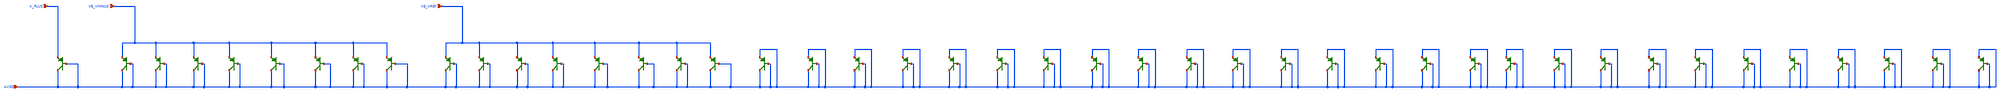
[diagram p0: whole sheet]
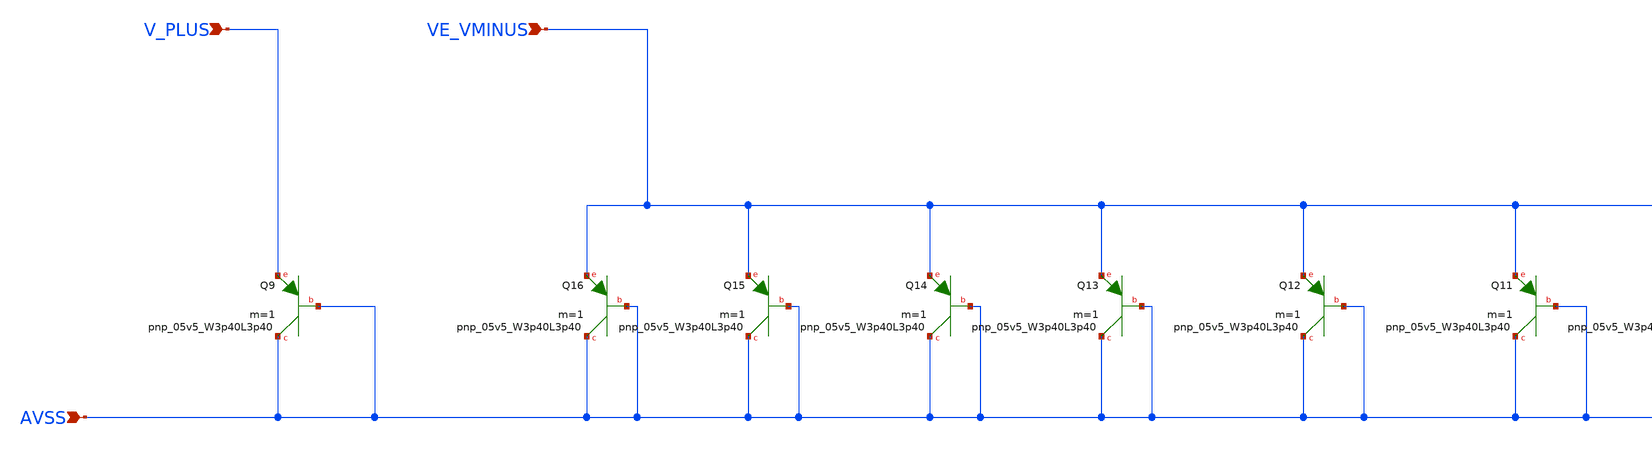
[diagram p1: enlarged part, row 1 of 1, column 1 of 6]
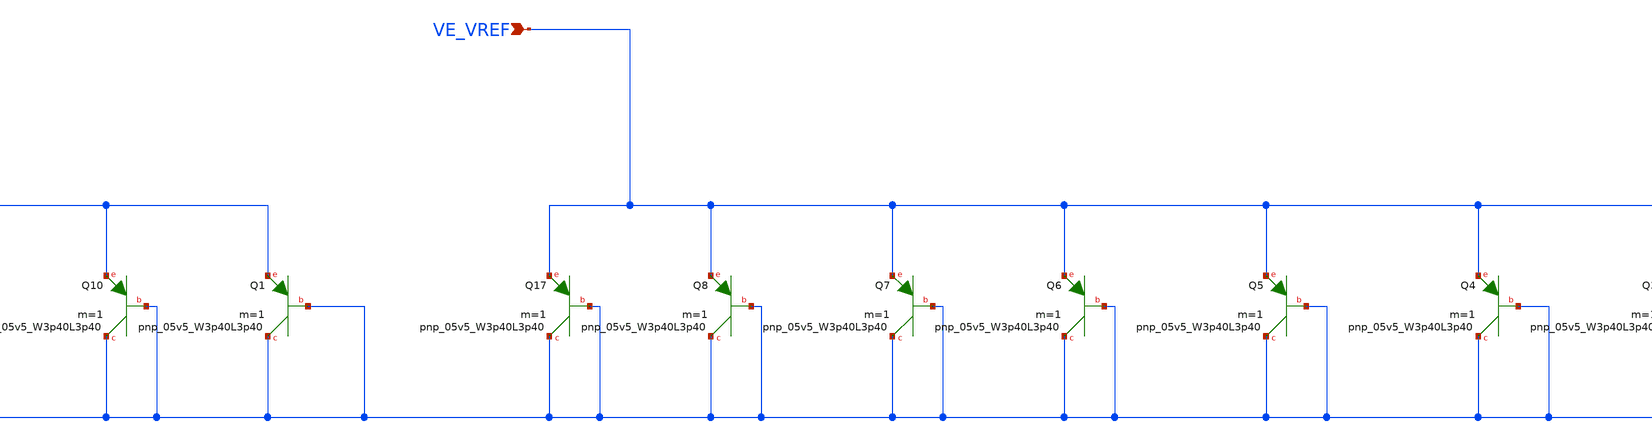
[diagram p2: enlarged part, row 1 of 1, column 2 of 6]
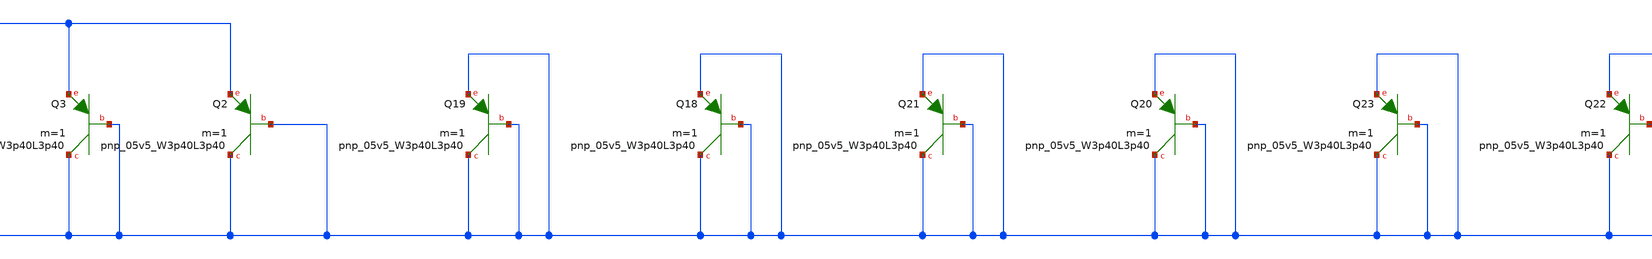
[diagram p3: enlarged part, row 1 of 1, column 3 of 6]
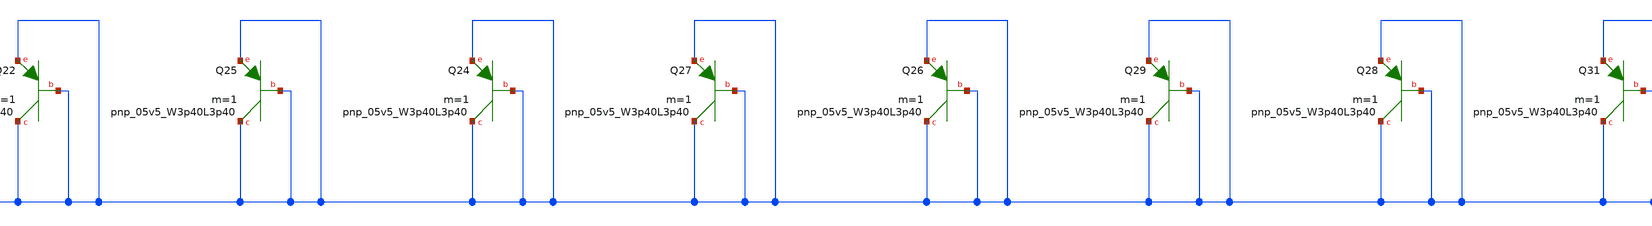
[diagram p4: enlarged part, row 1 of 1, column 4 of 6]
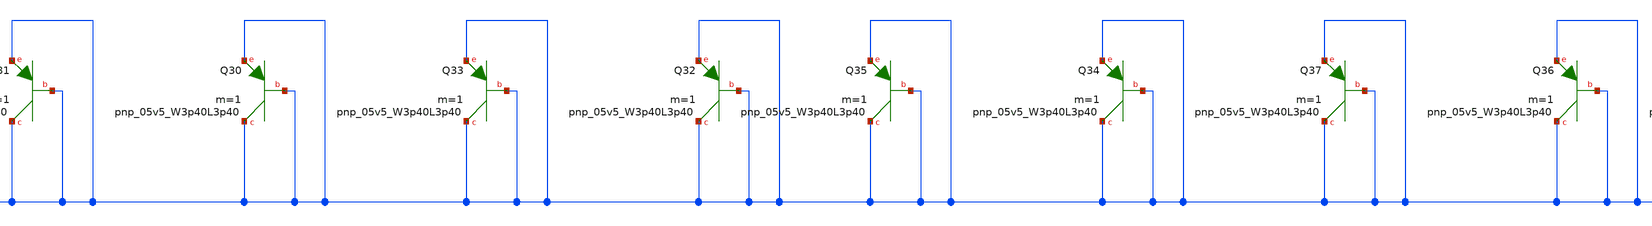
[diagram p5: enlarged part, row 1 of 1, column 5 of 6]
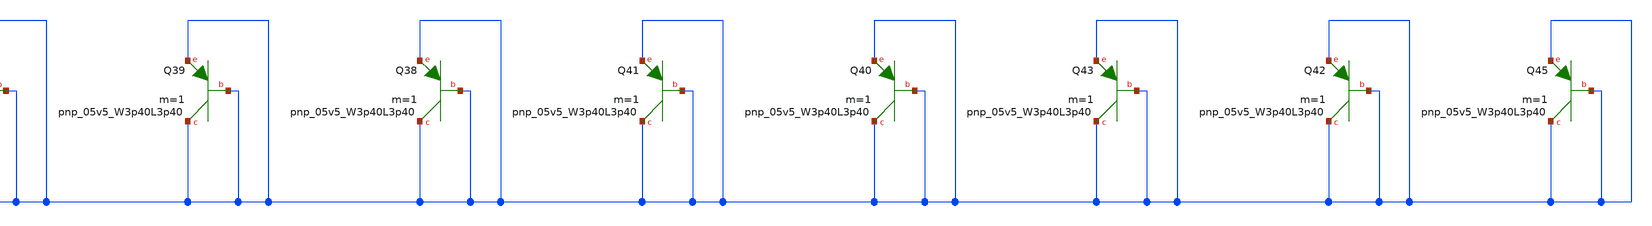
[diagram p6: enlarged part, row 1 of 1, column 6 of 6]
** sch_path: lef/lef/gds/bg2_bjt_array.sch
**.subckt bg2_bjt_array AVSS V_PLUS VE_VMINUS VE_VREF
*.ipin AVSS
*.ipin V_PLUS
*.ipin VE_VMINUS
*.ipin VE_VREF
XQ9 AVSS AVSS V_PLUS sky130_fd_pr__pnp_05v5_W3p40L3p40 m=1
XQ1 AVSS AVSS VE_VMINUS sky130_fd_pr__pnp_05v5_W3p40L3p40 m=1
XQ10 AVSS AVSS VE_VMINUS sky130_fd_pr__pnp_05v5_W3p40L3p40 m=1
XQ11 AVSS AVSS VE_VMINUS sky130_fd_pr__pnp_05v5_W3p40L3p40 m=1
XQ12 AVSS AVSS VE_VMINUS sky130_fd_pr__pnp_05v5_W3p40L3p40 m=1
XQ13 AVSS AVSS VE_VMINUS sky130_fd_pr__pnp_05v5_W3p40L3p40 m=1
XQ14 AVSS AVSS VE_VMINUS sky130_fd_pr__pnp_05v5_W3p40L3p40 m=1
XQ15 AVSS AVSS VE_VMINUS sky130_fd_pr__pnp_05v5_W3p40L3p40 m=1
XQ16 AVSS AVSS VE_VMINUS sky130_fd_pr__pnp_05v5_W3p40L3p40 m=1
XQ2 AVSS AVSS VE_VREF sky130_fd_pr__pnp_05v5_W3p40L3p40 m=1
XQ3 AVSS AVSS VE_VREF sky130_fd_pr__pnp_05v5_W3p40L3p40 m=1
XQ4 AVSS AVSS VE_VREF sky130_fd_pr__pnp_05v5_W3p40L3p40 m=1
XQ5 AVSS AVSS VE_VREF sky130_fd_pr__pnp_05v5_W3p40L3p40 m=1
XQ6 AVSS AVSS VE_VREF sky130_fd_pr__pnp_05v5_W3p40L3p40 m=1
XQ7 AVSS AVSS VE_VREF sky130_fd_pr__pnp_05v5_W3p40L3p40 m=1
XQ8 AVSS AVSS VE_VREF sky130_fd_pr__pnp_05v5_W3p40L3p40 m=1
XQ17 AVSS AVSS VE_VREF sky130_fd_pr__pnp_05v5_W3p40L3p40 m=1
XQ18 AVSS AVSS AVSS sky130_fd_pr__pnp_05v5_W3p40L3p40 m=1
XQ19 AVSS AVSS AVSS sky130_fd_pr__pnp_05v5_W3p40L3p40 m=1
XQ20 AVSS AVSS AVSS sky130_fd_pr__pnp_05v5_W3p40L3p40 m=1
XQ21 AVSS AVSS AVSS sky130_fd_pr__pnp_05v5_W3p40L3p40 m=1
XQ22 AVSS AVSS AVSS sky130_fd_pr__pnp_05v5_W3p40L3p40 m=1
XQ23 AVSS AVSS AVSS sky130_fd_pr__pnp_05v5_W3p40L3p40 m=1
XQ24 AVSS AVSS AVSS sky130_fd_pr__pnp_05v5_W3p40L3p40 m=1
XQ25 AVSS AVSS AVSS sky130_fd_pr__pnp_05v5_W3p40L3p40 m=1
XQ26 AVSS AVSS AVSS sky130_fd_pr__pnp_05v5_W3p40L3p40 m=1
XQ27 AVSS AVSS AVSS sky130_fd_pr__pnp_05v5_W3p40L3p40 m=1
XQ28 AVSS AVSS AVSS sky130_fd_pr__pnp_05v5_W3p40L3p40 m=1
XQ29 AVSS AVSS AVSS sky130_fd_pr__pnp_05v5_W3p40L3p40 m=1
XQ30 AVSS AVSS AVSS sky130_fd_pr__pnp_05v5_W3p40L3p40 m=1
XQ31 AVSS AVSS AVSS sky130_fd_pr__pnp_05v5_W3p40L3p40 m=1
XQ32 AVSS AVSS AVSS sky130_fd_pr__pnp_05v5_W3p40L3p40 m=1
XQ33 AVSS AVSS AVSS sky130_fd_pr__pnp_05v5_W3p40L3p40 m=1
XQ34 AVSS AVSS AVSS sky130_fd_pr__pnp_05v5_W3p40L3p40 m=1
XQ35 AVSS AVSS AVSS sky130_fd_pr__pnp_05v5_W3p40L3p40 m=1
XQ36 AVSS AVSS AVSS sky130_fd_pr__pnp_05v5_W3p40L3p40 m=1
XQ37 AVSS AVSS AVSS sky130_fd_pr__pnp_05v5_W3p40L3p40 m=1
XQ38 AVSS AVSS AVSS sky130_fd_pr__pnp_05v5_W3p40L3p40 m=1
XQ39 AVSS AVSS AVSS sky130_fd_pr__pnp_05v5_W3p40L3p40 m=1
XQ40 AVSS AVSS AVSS sky130_fd_pr__pnp_05v5_W3p40L3p40 m=1
XQ41 AVSS AVSS AVSS sky130_fd_pr__pnp_05v5_W3p40L3p40 m=1
XQ42 AVSS AVSS AVSS sky130_fd_pr__pnp_05v5_W3p40L3p40 m=1
XQ43 AVSS AVSS AVSS sky130_fd_pr__pnp_05v5_W3p40L3p40 m=1
XQ45 AVSS AVSS AVSS sky130_fd_pr__pnp_05v5_W3p40L3p40 m=1
**.ends
.end
